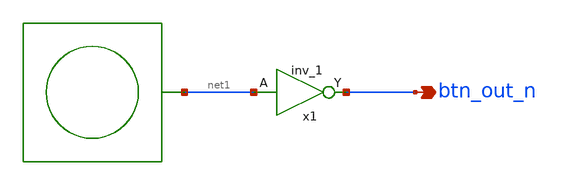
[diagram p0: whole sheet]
** sch_path: project/examples/button/button_test.sch
**.subckt button_test btn_out_n
*.opin btn_out_n
VBUTTON1 net1 VGND external
x1 net1 VGND VNB VPB VPWR btn_out_n sky130_fd_sc_hd__inv_1
**.ends
.end
